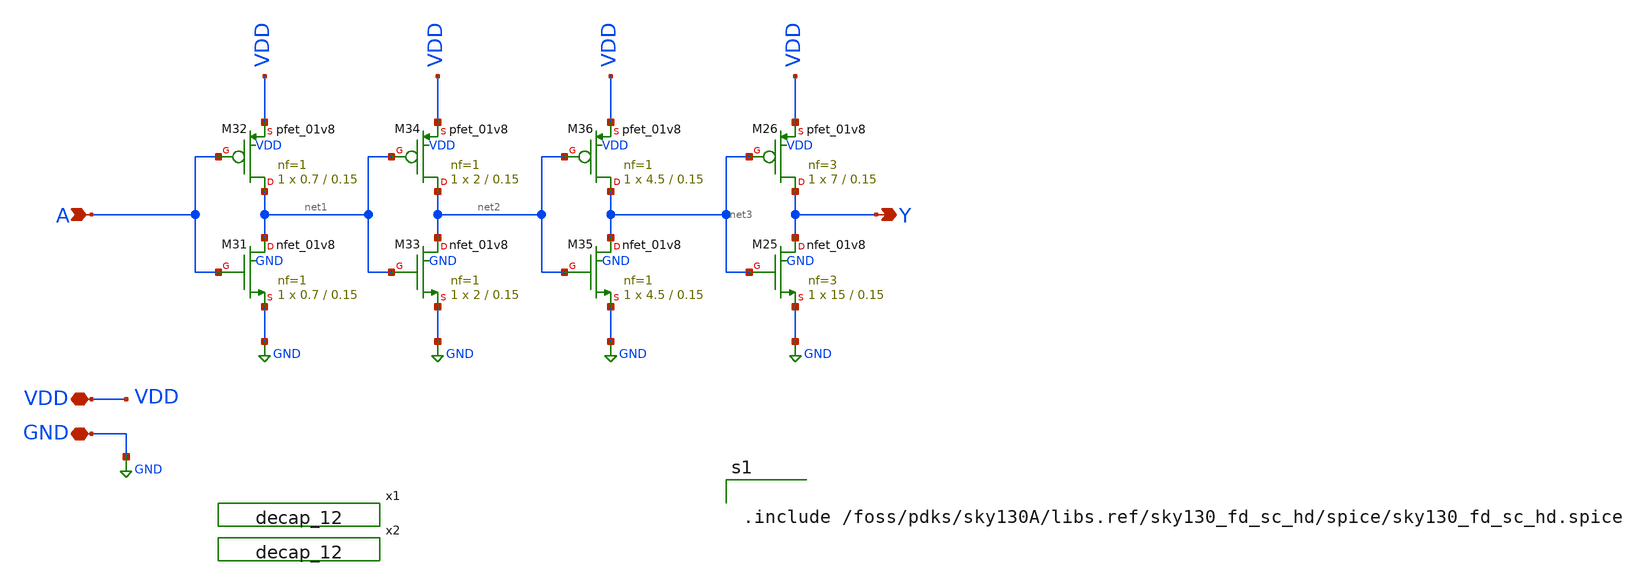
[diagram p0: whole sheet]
** sch_path: src/analog_source_files/output-buffer.sch
**.subckt output-buffer A Y VDD GND
*.ipin A
*.opin Y
*.iopin VDD
*.iopin GND
XM31 net1 A GND GND sky130_fd_pr__nfet_01v8 L=0.15 W=0.7 nf=1 ad='int((1 + 1)/2) * 0.7 / 1 * 0.29' as='int((1 + 2)/2) * 0.7 / 1 * 0.29'
+ pd='2*int((1 + 1)/2) * (0.7 / 1 + 0.29)' ps='2*int((1 + 2)/2) * (0.7 / 1 + 0.29)' nrd='0.29 / 0.7 ' nrs='0.29 / 0.7 '
+ sa=0 sb=0 sd=0 mult=1 m=1
XM32 net1 A VDD VDD sky130_fd_pr__pfet_01v8 L=0.15 W=0.7 nf=1 ad='int((1 + 1)/2) * 0.7 / 1 * 0.29' as='int((1 + 2)/2) * 0.7 / 1 * 0.29'
+ pd='2*int((1 + 1)/2) * (0.7 / 1 + 0.29)' ps='2*int((1 + 2)/2) * (0.7 / 1 + 0.29)' nrd='0.29 / 0.7 ' nrs='0.29 / 0.7 '
+ sa=0 sb=0 sd=0 mult=1 m=1
XM33 net2 net1 GND GND sky130_fd_pr__nfet_01v8 L=0.15 W=2 nf=1 ad='int((1 + 1)/2) * 2 / 1 * 0.29' as='int((1 + 2)/2) * 2 / 1 * 0.29'
+ pd='2*int((1 + 1)/2) * (2 / 1 + 0.29)' ps='2*int((1 + 2)/2) * (2 / 1 + 0.29)' nrd='0.29 / 2 ' nrs='0.29 / 2 '
+ sa=0 sb=0 sd=0 mult=1 m=1
XM34 net2 net1 VDD VDD sky130_fd_pr__pfet_01v8 L=0.15 W=2 nf=1 ad='int((1 + 1)/2) * 2 / 1 * 0.29' as='int((1 + 2)/2) * 2 / 1 * 0.29'
+ pd='2*int((1 + 1)/2) * (2 / 1 + 0.29)' ps='2*int((1 + 2)/2) * (2 / 1 + 0.29)' nrd='0.29 / 2 ' nrs='0.29 / 2 '
+ sa=0 sb=0 sd=0 mult=1 m=1
XM35 net3 net2 GND GND sky130_fd_pr__nfet_01v8 L=0.15 W=4.5 nf=1 ad='int((1 + 1)/2) * 4.5 / 1 * 0.29'
+ as='int((1 + 2)/2) * 4.5 / 1 * 0.29' pd='2*int((1 + 1)/2) * (4.5 / 1 + 0.29)' ps='2*int((1 + 2)/2) * (4.5 / 1 + 0.29)'
+ nrd='0.29 / 4.5 ' nrs='0.29 / 4.5 ' sa=0 sb=0 sd=0 mult=1 m=1
XM36 net3 net2 VDD VDD sky130_fd_pr__pfet_01v8 L=0.15 W=4.5 nf=1 ad='int((1 + 1)/2) * 4.5 / 1 * 0.29'
+ as='int((1 + 2)/2) * 4.5 / 1 * 0.29' pd='2*int((1 + 1)/2) * (4.5 / 1 + 0.29)' ps='2*int((1 + 2)/2) * (4.5 / 1 + 0.29)'
+ nrd='0.29 / 4.5 ' nrs='0.29 / 4.5 ' sa=0 sb=0 sd=0 mult=1 m=1
XM25 Y net3 GND GND sky130_fd_pr__nfet_01v8 L=0.15 W=15 nf=3 ad='int((3 + 1)/2) * 15 / 3 * 0.29' as='int((3 + 2)/2) * 15 / 3 * 0.29'
+ pd='2*int((3 + 1)/2) * (15 / 3 + 0.29)' ps='2*int((3 + 2)/2) * (15 / 3 + 0.29)' nrd='0.29 / 15 ' nrs='0.29 / 15 '
+ sa=0 sb=0 sd=0 mult=1 m=1
XM26 Y net3 VDD VDD sky130_fd_pr__pfet_01v8 L=0.15 W=7 nf=3 ad='int((3 + 1)/2) * 7 / 3 * 0.29' as='int((3 + 2)/2) * 7 / 3 * 0.29'
+ pd='2*int((3 + 1)/2) * (7 / 3 + 0.29)' ps='2*int((3 + 2)/2) * (7 / 3 + 0.29)' nrd='0.29 / 7 ' nrs='0.29 / 7 '
+ sa=0 sb=0 sd=0 mult=1 m=1
x1 GND GND VDD VDD sky130_fd_sc_hd__decap_12
x2 GND GND VDD VDD sky130_fd_sc_hd__decap_12
**** begin user architecture code


.include /foss/pdks/sky130A/libs.ref/sky130_fd_sc_hd/spice/sky130_fd_sc_hd.spice


**** end user architecture code
**.ends
.GLOBAL GND
.end
